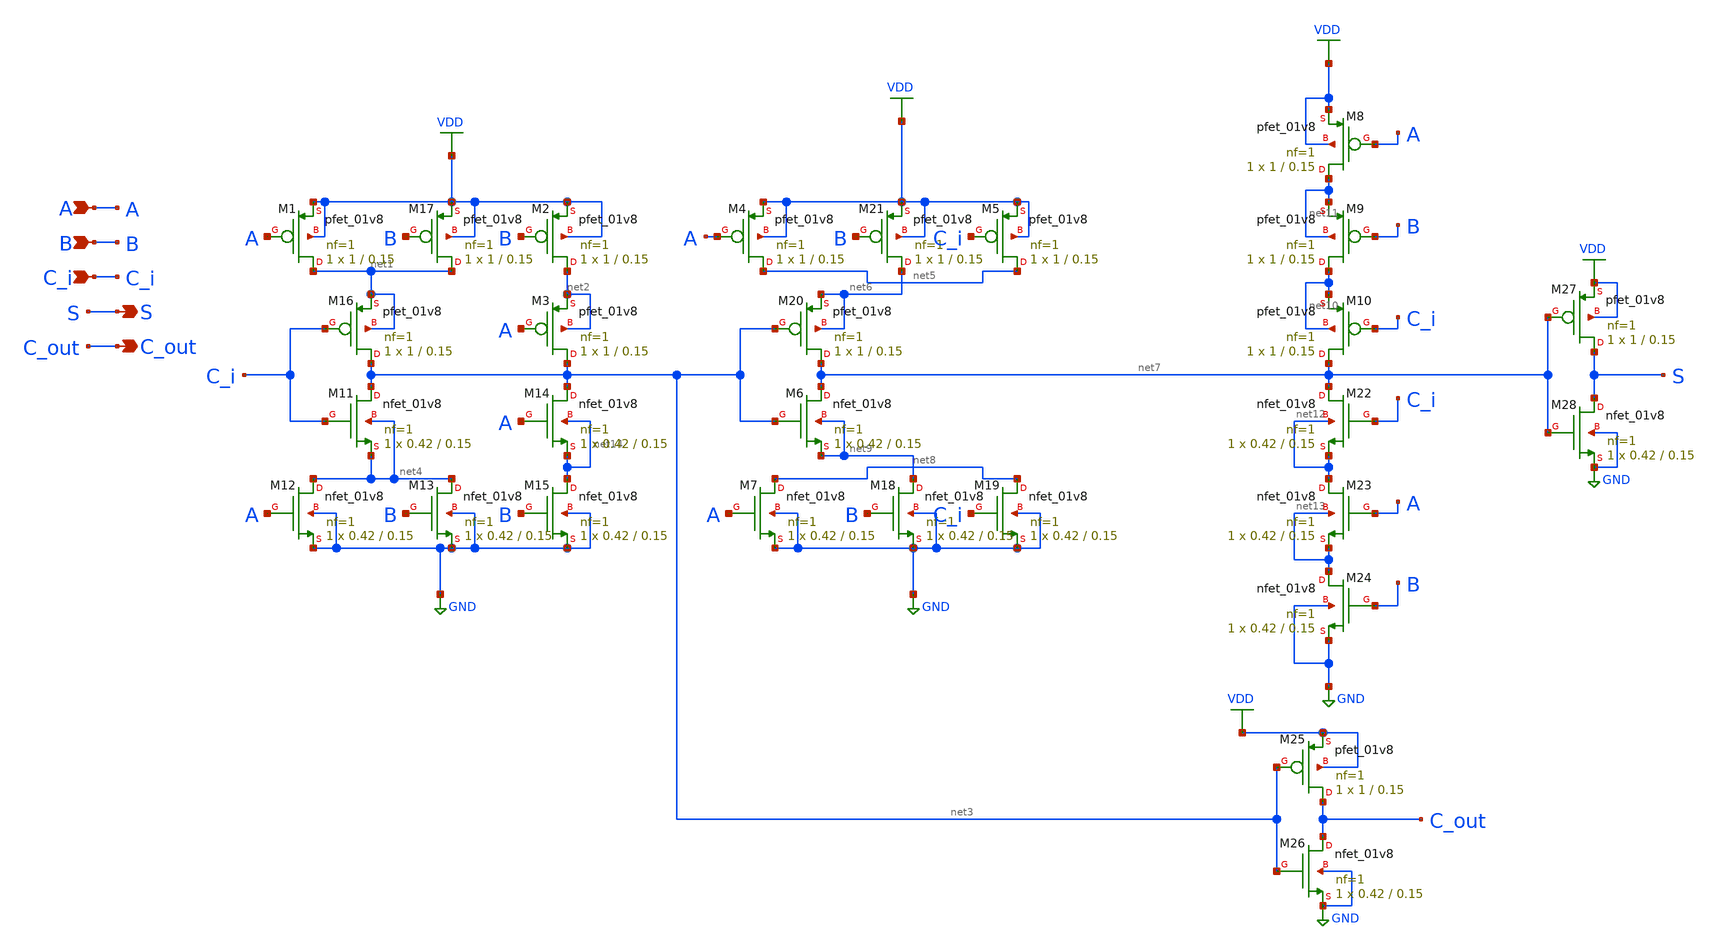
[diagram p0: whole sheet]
** sch_path: xschem/multi_input_addf.sch
**.subckt multi_input_addf A B C_i S C_out
*.ipin A
*.ipin B
*.ipin C_i
*.opin S
*.opin C_out
XM1 net1 A VDD VDD sky130_fd_pr__pfet_01v8 L=0.15 W=1 nf=1 ad='int((nf+1)/2) * W/nf * 0.29' as='int((nf+2)/2) * W/nf * 0.29'
+ pd='2*int((nf+1)/2) * (W/nf + 0.29)' ps='2*int((nf+2)/2) * (W/nf + 0.29)' nrd='0.29 / W' nrs='0.29 / W'
+ sa=0 sb=0 sd=0 mult=1 m=1
XM2 net2 B VDD VDD sky130_fd_pr__pfet_01v8 L=0.15 W=1 nf=1 ad='int((nf+1)/2) * W/nf * 0.29' as='int((nf+2)/2) * W/nf * 0.29'
+ pd='2*int((nf+1)/2) * (W/nf + 0.29)' ps='2*int((nf+2)/2) * (W/nf + 0.29)' nrd='0.29 / W' nrs='0.29 / W'
+ sa=0 sb=0 sd=0 mult=1 m=1
XM3 net3 A net2 net2 sky130_fd_pr__pfet_01v8 L=0.15 W=1 nf=1 ad='int((nf+1)/2) * W/nf * 0.29' as='int((nf+2)/2) * W/nf * 0.29'
+ pd='2*int((nf+1)/2) * (W/nf + 0.29)' ps='2*int((nf+2)/2) * (W/nf + 0.29)' nrd='0.29 / W' nrs='0.29 / W'
+ sa=0 sb=0 sd=0 mult=1 m=1
XM8 net11 A VDD VDD sky130_fd_pr__pfet_01v8 L=0.15 W=1 nf=1 ad='int((nf+1)/2) * W/nf * 0.29' as='int((nf+2)/2) * W/nf * 0.29'
+ pd='2*int((nf+1)/2) * (W/nf + 0.29)' ps='2*int((nf+2)/2) * (W/nf + 0.29)' nrd='0.29 / W' nrs='0.29 / W'
+ sa=0 sb=0 sd=0 mult=1 m=1
XM9 net10 B net11 net11 sky130_fd_pr__pfet_01v8 L=0.15 W=1 nf=1 ad='int((nf+1)/2) * W/nf * 0.29' as='int((nf+2)/2) * W/nf * 0.29'
+ pd='2*int((nf+1)/2) * (W/nf + 0.29)' ps='2*int((nf+2)/2) * (W/nf + 0.29)' nrd='0.29 / W' nrs='0.29 / W'
+ sa=0 sb=0 sd=0 mult=1 m=1
XM10 net7 C_i net10 net10 sky130_fd_pr__pfet_01v8 L=0.15 W=1 nf=1 ad='int((nf+1)/2) * W/nf * 0.29' as='int((nf+2)/2) * W/nf * 0.29'
+ pd='2*int((nf+1)/2) * (W/nf + 0.29)' ps='2*int((nf+2)/2) * (W/nf + 0.29)' nrd='0.29 / W' nrs='0.29 / W'
+ sa=0 sb=0 sd=0 mult=1 m=1
XM11 net3 C_i net4 net4 sky130_fd_pr__nfet_01v8 L=0.15 W=0.42 nf=1 ad='int((nf+1)/2) * W/nf * 0.29' as='int((nf+2)/2) * W/nf * 0.29'
+ pd='2*int((nf+1)/2) * (W/nf + 0.29)' ps='2*int((nf+2)/2) * (W/nf + 0.29)' nrd='0.29 / W' nrs='0.29 / W'
+ sa=0 sb=0 sd=0 mult=1 m=1
XM12 net4 A GND GND sky130_fd_pr__nfet_01v8 L=0.15 W=0.42 nf=1 ad='int((nf+1)/2) * W/nf * 0.29' as='int((nf+2)/2) * W/nf * 0.29'
+ pd='2*int((nf+1)/2) * (W/nf + 0.29)' ps='2*int((nf+2)/2) * (W/nf + 0.29)' nrd='0.29 / W' nrs='0.29 / W'
+ sa=0 sb=0 sd=0 mult=1 m=1
XM13 net4 B GND GND sky130_fd_pr__nfet_01v8 L=0.15 W=0.42 nf=1 ad='int((nf+1)/2) * W/nf * 0.29' as='int((nf+2)/2) * W/nf * 0.29'
+ pd='2*int((nf+1)/2) * (W/nf + 0.29)' ps='2*int((nf+2)/2) * (W/nf + 0.29)' nrd='0.29 / W' nrs='0.29 / W'
+ sa=0 sb=0 sd=0 mult=1 m=1
XM14 net3 A net14 net14 sky130_fd_pr__nfet_01v8 L=0.15 W=0.42 nf=1 ad='int((nf+1)/2) * W/nf * 0.29' as='int((nf+2)/2) * W/nf * 0.29'
+ pd='2*int((nf+1)/2) * (W/nf + 0.29)' ps='2*int((nf+2)/2) * (W/nf + 0.29)' nrd='0.29 / W' nrs='0.29 / W'
+ sa=0 sb=0 sd=0 mult=1 m=1
XM15 net14 B GND GND sky130_fd_pr__nfet_01v8 L=0.15 W=0.42 nf=1 ad='int((nf+1)/2) * W/nf * 0.29' as='int((nf+2)/2) * W/nf * 0.29'
+ pd='2*int((nf+1)/2) * (W/nf + 0.29)' ps='2*int((nf+2)/2) * (W/nf + 0.29)' nrd='0.29 / W' nrs='0.29 / W'
+ sa=0 sb=0 sd=0 mult=1 m=1
XM16 net3 C_i net1 net1 sky130_fd_pr__pfet_01v8 L=0.15 W=1 nf=1 ad='int((nf+1)/2) * W/nf * 0.29' as='int((nf+2)/2) * W/nf * 0.29'
+ pd='2*int((nf+1)/2) * (W/nf + 0.29)' ps='2*int((nf+2)/2) * (W/nf + 0.29)' nrd='0.29 / W' nrs='0.29 / W'
+ sa=0 sb=0 sd=0 mult=1 m=1
XM17 net1 B VDD VDD sky130_fd_pr__pfet_01v8 L=0.15 W=1 nf=1 ad='int((nf+1)/2) * W/nf * 0.29' as='int((nf+2)/2) * W/nf * 0.29'
+ pd='2*int((nf+1)/2) * (W/nf + 0.29)' ps='2*int((nf+2)/2) * (W/nf + 0.29)' nrd='0.29 / W' nrs='0.29 / W'
+ sa=0 sb=0 sd=0 mult=1 m=1
XM4 net5 A VDD VDD sky130_fd_pr__pfet_01v8 L=0.15 W=1 nf=1 ad='int((nf+1)/2) * W/nf * 0.29' as='int((nf+2)/2) * W/nf * 0.29'
+ pd='2*int((nf+1)/2) * (W/nf + 0.29)' ps='2*int((nf+2)/2) * (W/nf + 0.29)' nrd='0.29 / W' nrs='0.29 / W'
+ sa=0 sb=0 sd=0 mult=1 m=1
XM5 net5 C_i VDD VDD sky130_fd_pr__pfet_01v8 L=0.15 W=1 nf=1 ad='int((nf+1)/2) * W/nf * 0.29' as='int((nf+2)/2) * W/nf * 0.29'
+ pd='2*int((nf+1)/2) * (W/nf + 0.29)' ps='2*int((nf+2)/2) * (W/nf + 0.29)' nrd='0.29 / W' nrs='0.29 / W'
+ sa=0 sb=0 sd=0 mult=1 m=1
XM6 net7 net3 net9 net9 sky130_fd_pr__nfet_01v8 L=0.15 W=0.42 nf=1 ad='int((nf+1)/2) * W/nf * 0.29' as='int((nf+2)/2) * W/nf * 0.29'
+ pd='2*int((nf+1)/2) * (W/nf + 0.29)' ps='2*int((nf+2)/2) * (W/nf + 0.29)' nrd='0.29 / W' nrs='0.29 / W'
+ sa=0 sb=0 sd=0 mult=1 m=1
XM7 net8 A GND GND sky130_fd_pr__nfet_01v8 L=0.15 W=0.42 nf=1 ad='int((nf+1)/2) * W/nf * 0.29' as='int((nf+2)/2) * W/nf * 0.29'
+ pd='2*int((nf+1)/2) * (W/nf + 0.29)' ps='2*int((nf+2)/2) * (W/nf + 0.29)' nrd='0.29 / W' nrs='0.29 / W'
+ sa=0 sb=0 sd=0 mult=1 m=1
XM18 net9 B GND GND sky130_fd_pr__nfet_01v8 L=0.15 W=0.42 nf=1 ad='int((nf+1)/2) * W/nf * 0.29' as='int((nf+2)/2) * W/nf * 0.29'
+ pd='2*int((nf+1)/2) * (W/nf + 0.29)' ps='2*int((nf+2)/2) * (W/nf + 0.29)' nrd='0.29 / W' nrs='0.29 / W'
+ sa=0 sb=0 sd=0 mult=1 m=1
XM19 net8 C_i GND GND sky130_fd_pr__nfet_01v8 L=0.15 W=0.42 nf=1 ad='int((nf+1)/2) * W/nf * 0.29' as='int((nf+2)/2) * W/nf * 0.29'
+ pd='2*int((nf+1)/2) * (W/nf + 0.29)' ps='2*int((nf+2)/2) * (W/nf + 0.29)' nrd='0.29 / W' nrs='0.29 / W'
+ sa=0 sb=0 sd=0 mult=1 m=1
XM20 net7 net3 net6 net6 sky130_fd_pr__pfet_01v8 L=0.15 W=1 nf=1 ad='int((nf+1)/2) * W/nf * 0.29' as='int((nf+2)/2) * W/nf * 0.29'
+ pd='2*int((nf+1)/2) * (W/nf + 0.29)' ps='2*int((nf+2)/2) * (W/nf + 0.29)' nrd='0.29 / W' nrs='0.29 / W'
+ sa=0 sb=0 sd=0 mult=1 m=1
XM21 net6 B VDD VDD sky130_fd_pr__pfet_01v8 L=0.15 W=1 nf=1 ad='int((nf+1)/2) * W/nf * 0.29' as='int((nf+2)/2) * W/nf * 0.29'
+ pd='2*int((nf+1)/2) * (W/nf + 0.29)' ps='2*int((nf+2)/2) * (W/nf + 0.29)' nrd='0.29 / W' nrs='0.29 / W'
+ sa=0 sb=0 sd=0 mult=1 m=1
XM22 net7 C_i net12 net12 sky130_fd_pr__nfet_01v8 L=0.15 W=0.42 nf=1 ad='int((nf+1)/2) * W/nf * 0.29'
+ as='int((nf+2)/2) * W/nf * 0.29' pd='2*int((nf+1)/2) * (W/nf + 0.29)' ps='2*int((nf+2)/2) * (W/nf + 0.29)'
+ nrd='0.29 / W' nrs='0.29 / W' sa=0 sb=0 sd=0 mult=1 m=1
XM23 net12 A net13 net13 sky130_fd_pr__nfet_01v8 L=0.15 W=0.42 nf=1 ad='int((nf+1)/2) * W/nf * 0.29'
+ as='int((nf+2)/2) * W/nf * 0.29' pd='2*int((nf+1)/2) * (W/nf + 0.29)' ps='2*int((nf+2)/2) * (W/nf + 0.29)'
+ nrd='0.29 / W' nrs='0.29 / W' sa=0 sb=0 sd=0 mult=1 m=1
XM24 net13 B GND GND sky130_fd_pr__nfet_01v8 L=0.15 W=0.42 nf=1 ad='int((nf+1)/2) * W/nf * 0.29' as='int((nf+2)/2) * W/nf * 0.29'
+ pd='2*int((nf+1)/2) * (W/nf + 0.29)' ps='2*int((nf+2)/2) * (W/nf + 0.29)' nrd='0.29 / W' nrs='0.29 / W'
+ sa=0 sb=0 sd=0 mult=1 m=1
XM25 C_out net3 VDD VDD sky130_fd_pr__pfet_01v8 L=0.15 W=1 nf=1 ad='int((nf+1)/2) * W/nf * 0.29' as='int((nf+2)/2) * W/nf * 0.29'
+ pd='2*int((nf+1)/2) * (W/nf + 0.29)' ps='2*int((nf+2)/2) * (W/nf + 0.29)' nrd='0.29 / W' nrs='0.29 / W'
+ sa=0 sb=0 sd=0 mult=1 m=1
XM26 C_out net3 GND GND sky130_fd_pr__nfet_01v8 L=0.15 W=0.42 nf=1 ad='int((nf+1)/2) * W/nf * 0.29' as='int((nf+2)/2) * W/nf * 0.29'
+ pd='2*int((nf+1)/2) * (W/nf + 0.29)' ps='2*int((nf+2)/2) * (W/nf + 0.29)' nrd='0.29 / W' nrs='0.29 / W'
+ sa=0 sb=0 sd=0 mult=1 m=1
XM27 S net7 VDD VDD sky130_fd_pr__pfet_01v8 L=0.15 W=1 nf=1 ad='int((nf+1)/2) * W/nf * 0.29' as='int((nf+2)/2) * W/nf * 0.29'
+ pd='2*int((nf+1)/2) * (W/nf + 0.29)' ps='2*int((nf+2)/2) * (W/nf + 0.29)' nrd='0.29 / W' nrs='0.29 / W'
+ sa=0 sb=0 sd=0 mult=1 m=1
XM28 S net7 GND GND sky130_fd_pr__nfet_01v8 L=0.15 W=0.42 nf=1 ad='int((nf+1)/2) * W/nf * 0.29' as='int((nf+2)/2) * W/nf * 0.29'
+ pd='2*int((nf+1)/2) * (W/nf + 0.29)' ps='2*int((nf+2)/2) * (W/nf + 0.29)' nrd='0.29 / W' nrs='0.29 / W'
+ sa=0 sb=0 sd=0 mult=1 m=1
**.ends
.GLOBAL VDD
.GLOBAL GND
.end
